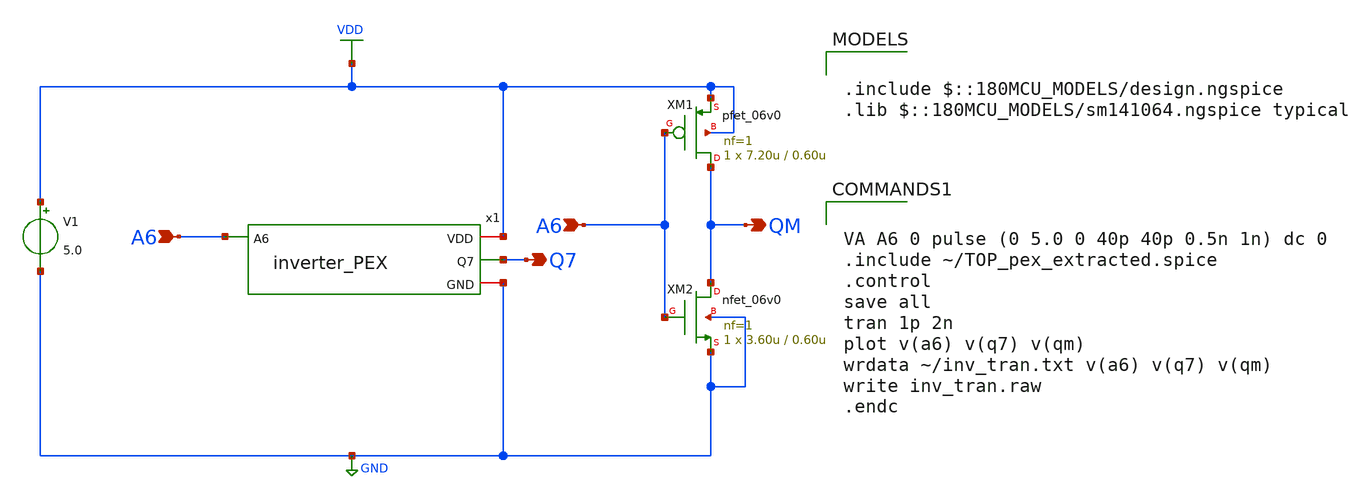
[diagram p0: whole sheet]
** sch_path: member_project/noritsuna/inverter/xschem/inverter_PEX_testbench.sch
**.subckt inverter_PEX_testbench A6 Q7 A6 QM
*.ipin A6
*.opin Q7
*.ipin A6
*.opin QM
V1 VDD GND 5.0
x1 VDD GND A6 Q7 TOP
XM1 QM A6 VDD VDD pfet_06v0 L=0.60u W=7.20u nf=1 ad='int((nf+1)/2) * W/nf * 0.18u' as='int((nf+2)/2) * W/nf * 0.18u'
+ pd='2*int((nf+1)/2) * (W/nf + 0.18u)' ps='2*int((nf+2)/2) * (W/nf + 0.18u)' nrd='0.18u / W' nrs='0.18u / W'
+ sa=0 sb=0 sd=0 m=1
XM2 QM A6 GND GND nfet_06v0 L=0.60u W=3.60u nf=1 ad='int((nf+1)/2) * W/nf * 0.18u' as='int((nf+2)/2) * W/nf * 0.18u'
+ pd='2*int((nf+1)/2) * (W/nf + 0.18u)' ps='2*int((nf+2)/2) * (W/nf + 0.18u)' nrd='0.18u / W' nrs='0.18u / W'
+ sa=0 sb=0 sd=0 m=1
**** begin user architecture code

.include $::180MCU_MODELS/design.ngspice
.lib $::180MCU_MODELS/sm141064.ngspice typical



VA A6 0 pulse (0 5.0 0 40p 40p 0.5n 1n) dc 0
.include ~/TOP_pex_extracted.spice
.control
save all
tran 1p 2n
plot v(a6) v(q7) v(qm)
wrdata ~/inv_tran.txt v(a6) v(q7) v(qm)
write inv_tran.raw
.endc


**** end user architecture code
**.ends
.GLOBAL GND
.GLOBAL VDD
.end
